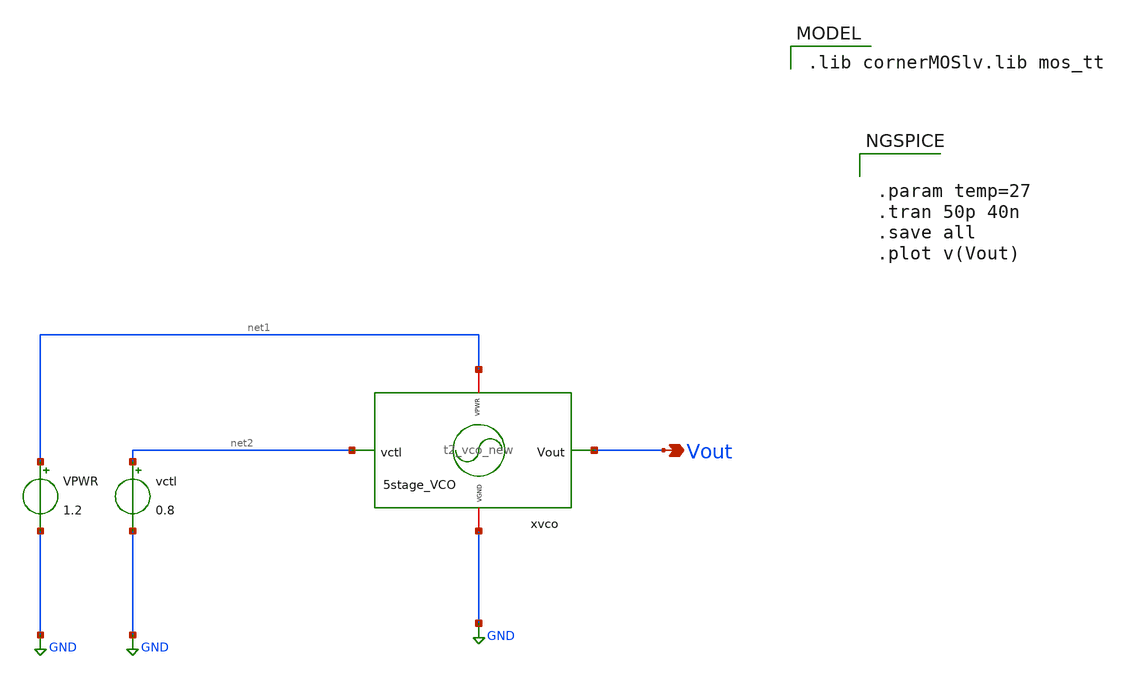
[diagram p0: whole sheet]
** sch_path: Team 2 Design/design_data/xschem/t2_vco_new_tb_.sch
**.subckt t2_vco_new_tb_ Vout
*.opin Vout
x1 net1 GND net2 Vout t2_vco_new
VPWR net1 GND 1.2
vctl net2 GND 0.8
**** begin user architecture code
 .lib cornerMOSlv.lib mos_tt



.param temp=27
.tran 50p 40n
.save all
.plot v(Vout)


**** end user architecture code
**.ends
.GLOBAL GND
.end
